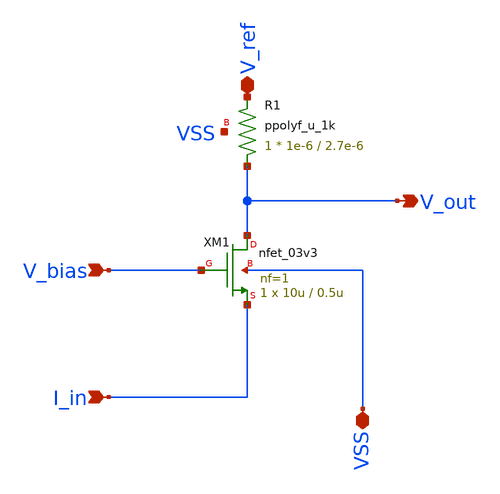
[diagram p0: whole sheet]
** sch_path: schematics/cg_amp_tia.sch
**.subckt cg_amp_tia V_ref VSS I_in V_bias V_out
*.iopin V_ref
*.iopin VSS
*.ipin I_in
*.ipin V_bias
*.opin V_out
XM1 V_out V_bias I_in VSS nfet_03v3 L=0.5u W=10u nf=1 ad='int((nf+1)/2) * W/nf * 0.18u' as='int((nf+2)/2) * W/nf * 0.18u'
+ pd='2*int((nf+1)/2) * (W/nf + 0.18u)' ps='2*int((nf+2)/2) * (W/nf + 0.18u)' nrd='0.18u / W' nrs='0.18u / W'
+ sa=0 sb=0 sd=0 m=1
XR1 V_out V_ref VSS ppolyf_u_1k r_width=1e-6 r_length=2.7e-6 m=1
**.ends
.end
